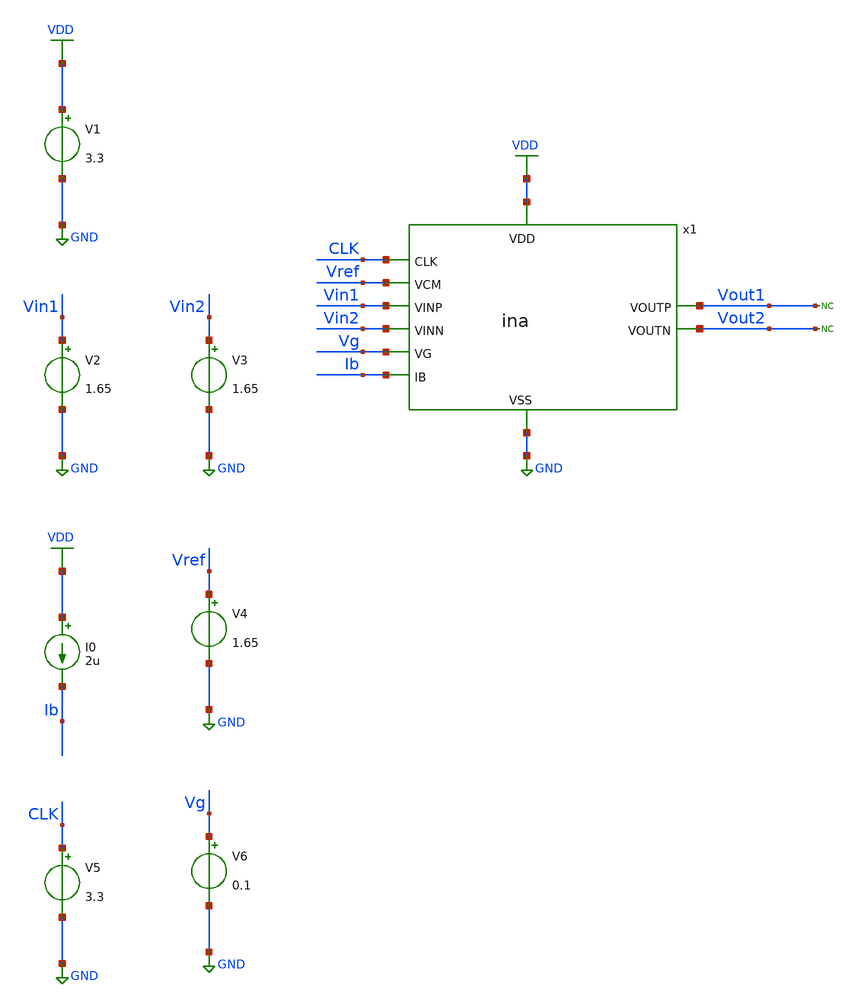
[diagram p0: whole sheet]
** sch_path: designs/libs/tb_ina/tb_ina_noise/tb_ina_noise.sch
**.subckt tb_ina_noise
V1 VDD GND 3.3
V2 Vin1 GND 1.65
V3 Vin2 GND 1.65
I0 VDD Ib 2u
V4 Vref GND 1.65
V5 CLK GND 3.3
V6 Vg GND 0.1
* noconn Vout1
* noconn Vout2
x1 Vg VDD Vin1 Vin2 CLK Vout1 Vout2 GND Vref Ib ina
**** begin user architecture code

.include $::180MCU_MODELS/design.ngspice
.lib $::180MCU_MODELS/sm141064.ngspice typical
.lib $::180MCU_MODELS/sm141064.ngspice cap_mim
.lib $::180MCU_MODELS/sm141064.ngspice moscap_typical
.lib $::180MCU_MODELS/sm141064.ngspice mimcap_typical
.lib $::180MCU_MODELS/sm141064.ngspice res_typical
* .lib $::180MCU_MODELS/sm141064.ngspice res_statistical
* ngspice commands




.control
save all

run
set color0 = white

*************************************
** PARAMETERS
*************************************

let Vdd  = 3.3
let Vcm  = Vdd/2
let Ibias = 2u
let Vg = 0.1

*************************************
** CHOPPER PARAMETERS
*************************************

let fchop = 4k
let tper = 1/fchop
let ton = tper/2
let tr = 10n
let tf = 10n

*************************************
** SOURCES
*************************************

alter @V1[DC] = $&Vdd
alter @V2[DC] = $&Vcm
alter @V3[DC] = $&Vcm
alter @V2[ACMAG] = 1
alter @V3[ACMAG] = 0
alter @V4[DC] = $&Vcm
alter @I0[DC] = $&Ibias
alter @V5[PULSE] = [ 0 $&Vdd 0 $&tr $&tf $&ton $&tper 0 ]
alter @V6[DC] = $&Vg

*************************************
** NOISE SIMULATION
*************************************

op
noise v(Vout1) V2 dec 100 0.01 1G

*************************************
** PLOTS
*************************************

setplot noise1
plot onoise_spectrum
plot inoise_spectrum

*************************************
** MEASUREMENTS
*************************************

* Input Noise Density
let inoise_1Hz   = inoise_spectrum[200]
let inoise_10Hz  = inoise_spectrum[300]
let inoise_100Hz = inoise_spectrum[400]
print inoise_1Hz
print inoise_10Hz
print inoise_100Hz
* Output Noise Density
let onoise_1Hz = onoise_spectrum[200]
let onoise_10Hz = onoise_spectrum[300]
let onoise_100Hz = onoise_spectrum[400]
print onoise_1Hz
print onoise_10Hz
print onoise_100Hz

*************************************
** SAVE
*************************************

write tb_ina_noise.raw

*************************************
** NOISE SIMULATION2
*************************************

noise v(Vout1) V2 dec 500 0.5 150

setplot noise4
* Integrated Input-Referred Noise (0.5 Hz - 150 Hz)
let inoise_rms = inoise_total
print inoise_rms
* Integrated Output Noise (0.5 Hz - 150 Hz)
let onoise_rms = onoise_total
print onoise_rms

.endc
* ngspice commands



**** end user architecture code
**.ends
.GLOBAL GND
.GLOBAL VDD
.end
